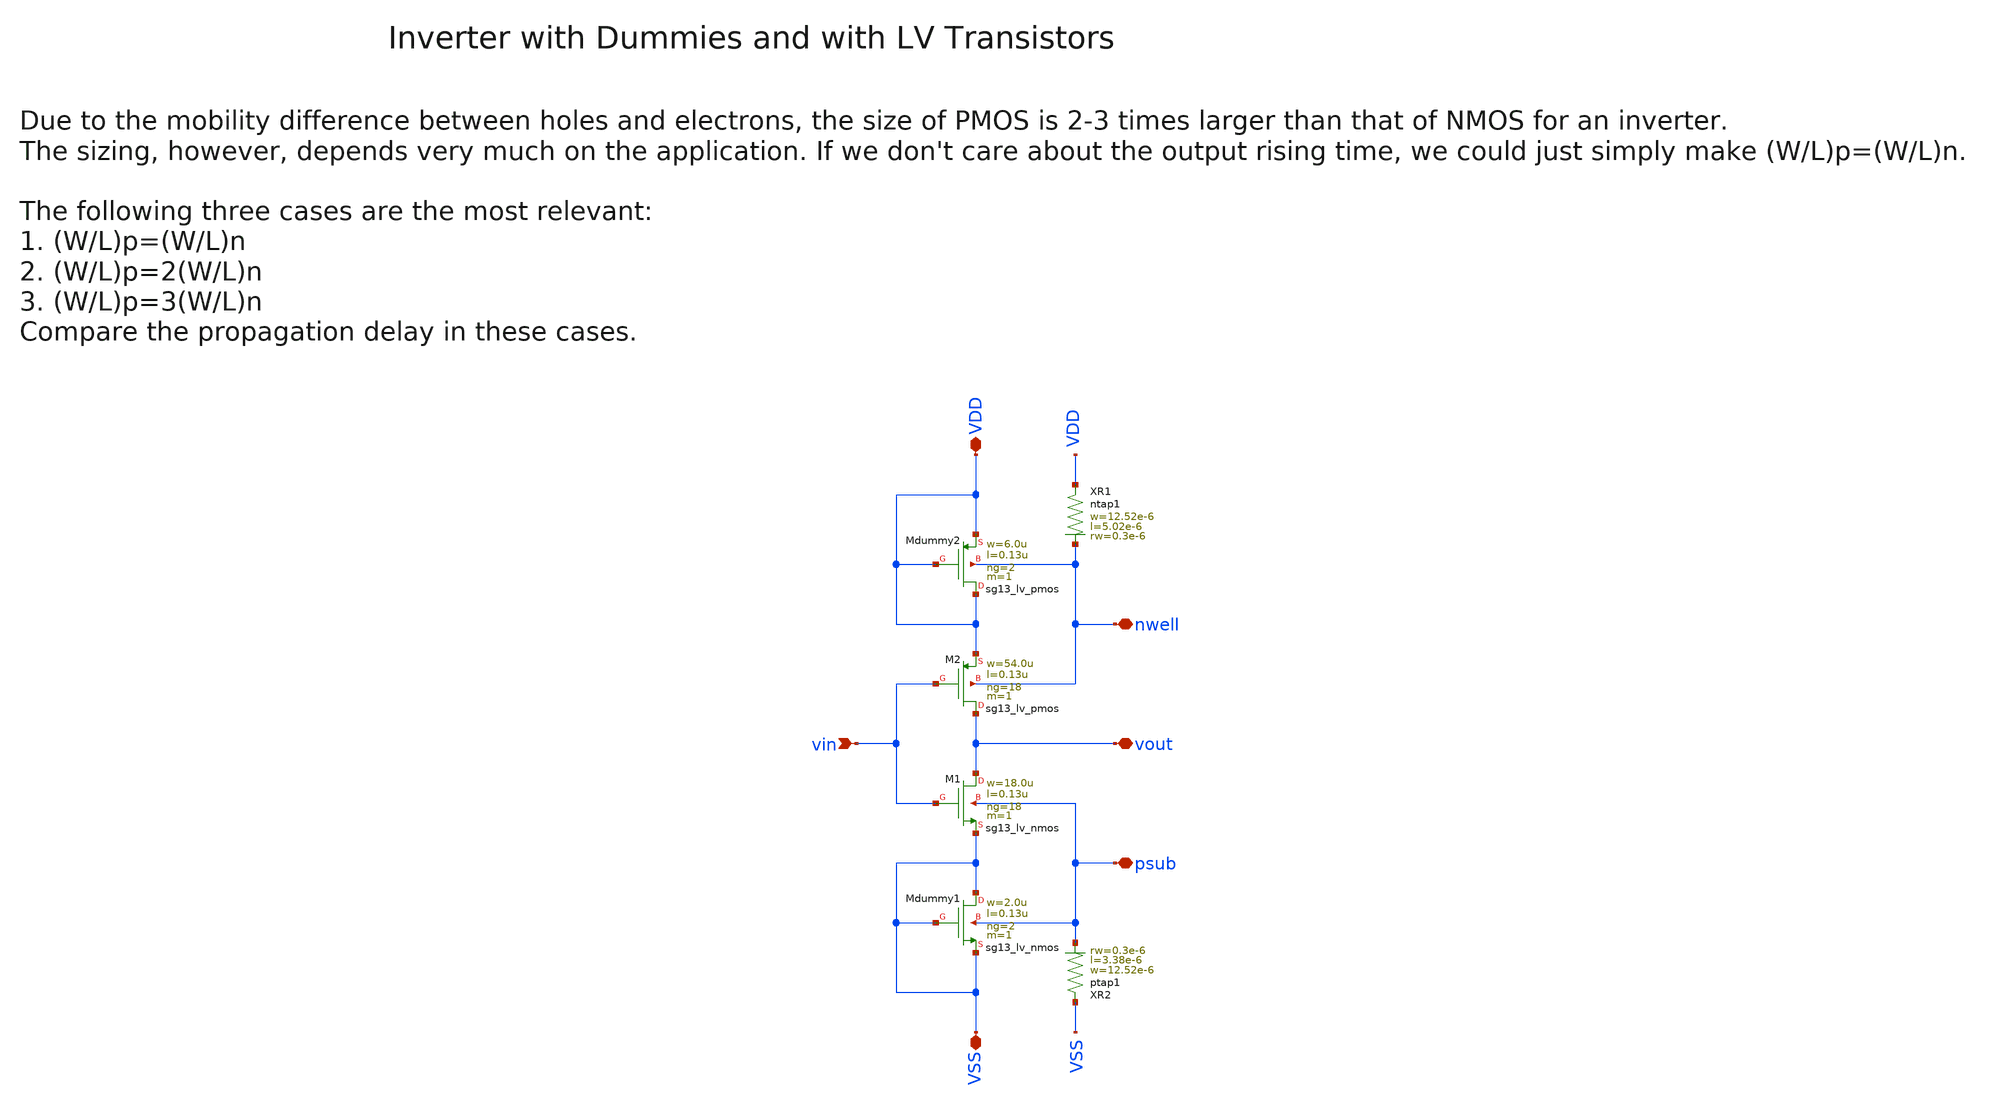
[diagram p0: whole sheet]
** sch_path: ihp130/macros/iqmod/xschem/iqmod_mixer_se2diff_inv_NF18.sch
**.subckt iqmod_mixer_se2diff_inv_NF18 vin VDD VSS vout nwell psub
*.ipin vin
*.iopin VDD
*.iopin VSS
*.iopin vout
*.iopin nwell
*.iopin psub
XM1 vout vin VSS psub sg13_lv_nmos w=18.0u l=0.13u ng=18 m=1 mm_ok=1
XM2 vout vin VDD nwell sg13_lv_pmos w=54.0u l=0.13u ng=18 m=1 mm_ok=1
XMdummy1 VSS VSS VSS psub sg13_lv_nmos w=2.0u l=0.13u ng=2 m=1 mm_ok=1
XMdummy2 VDD VDD VDD nwell sg13_lv_pmos w=6.0u l=0.13u ng=2 m=1 mm_ok=1
XR1 VDD nwell ntap1 R=6.727 w=12.52e-6 l=5.02e-6 rw=0.3e-6
XR2 VSS psub ptap1 R=7.448 w=12.52e-6 l=3.38e-6 rw=0.3e-6
**.ends
.end
